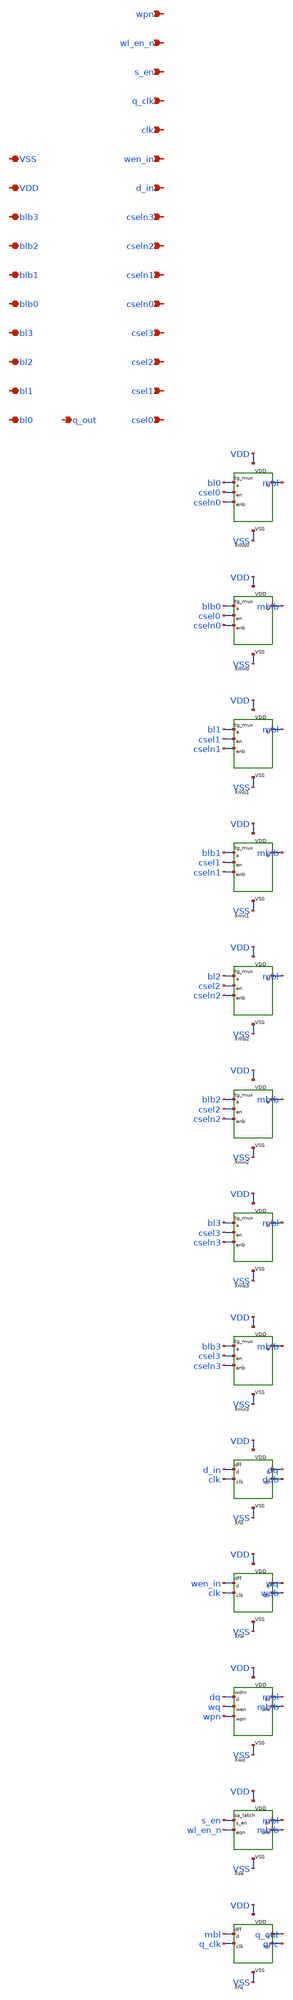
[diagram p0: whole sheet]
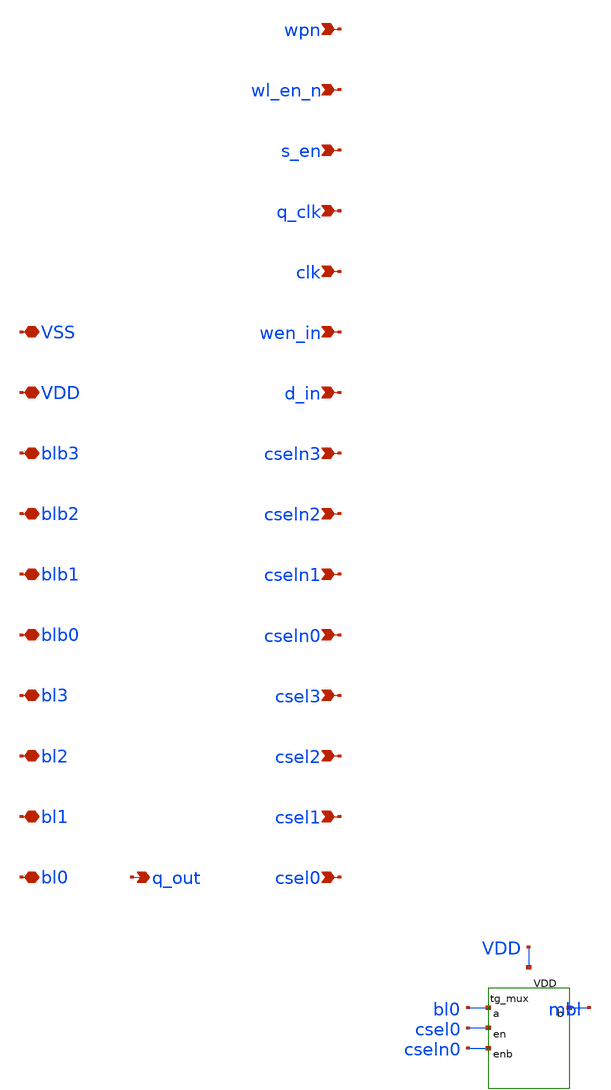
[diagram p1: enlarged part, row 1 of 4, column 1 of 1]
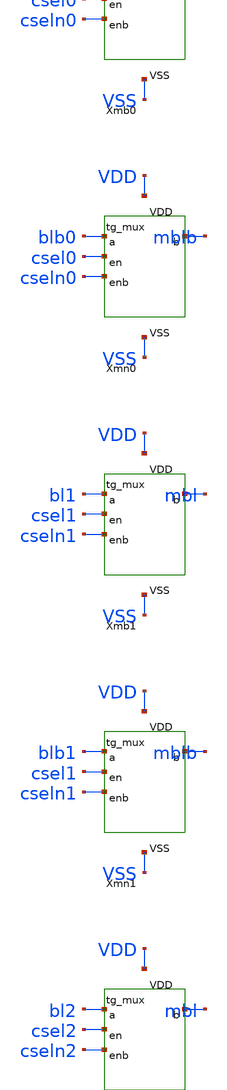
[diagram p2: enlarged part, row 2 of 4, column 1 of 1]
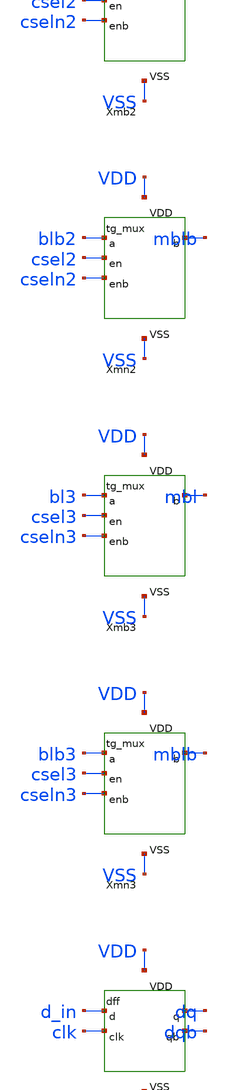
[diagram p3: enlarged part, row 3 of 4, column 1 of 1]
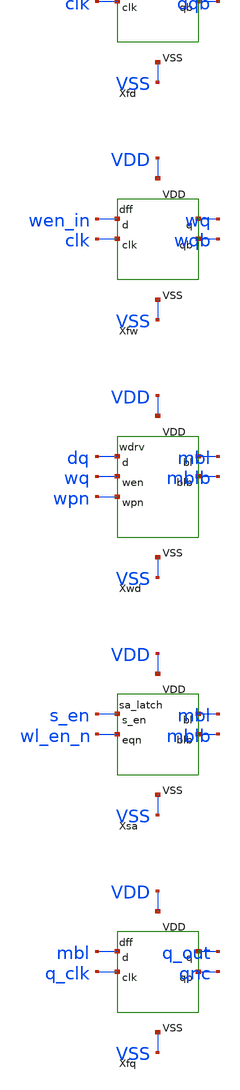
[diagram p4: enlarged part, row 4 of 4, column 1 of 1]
** sch_path: design/io_slice.sch
**.subckt io_slice csel0 csel1 csel2 csel3 cseln0 cseln1 cseln2 cseln3 d_in wen_in clk q_clk s_en
*+ wl_en_n wpn q_out bl0 bl1 bl2 bl3 blb0 blb1 blb2 blb3 VDD VSS
*.ipin csel0
*.ipin csel1
*.ipin csel2
*.ipin csel3
*.ipin cseln0
*.ipin cseln1
*.ipin cseln2
*.ipin cseln3
*.ipin d_in
*.ipin wen_in
*.ipin clk
*.ipin q_clk
*.ipin s_en
*.ipin wl_en_n
*.ipin wpn
*.opin q_out
*.iopin bl0
*.iopin bl1
*.iopin bl2
*.iopin bl3
*.iopin blb0
*.iopin blb1
*.iopin blb2
*.iopin blb3
*.iopin VDD
*.iopin VSS
XXmb0 bl0 csel0 cseln0 mbl VDD VSS tg_mux
XXmn0 blb0 csel0 cseln0 mblb VDD VSS tg_mux
XXmb1 bl1 csel1 cseln1 mbl VDD VSS tg_mux
XXmn1 blb1 csel1 cseln1 mblb VDD VSS tg_mux
XXmb2 bl2 csel2 cseln2 mbl VDD VSS tg_mux
XXmn2 blb2 csel2 cseln2 mblb VDD VSS tg_mux
XXmb3 bl3 csel3 cseln3 mbl VDD VSS tg_mux
XXmn3 blb3 csel3 cseln3 mblb VDD VSS tg_mux
XXfd d_in clk dq dqb VDD VSS dff
XXfw wen_in clk wq wqb VDD VSS dff
XXwd dq wq wpn mbl mblb VDD VSS wdrv
XXsa s_en wl_en_n mbl mblb VDD VSS sa_latch
XXfq mbl q_clk q_out qnc VDD VSS dff
**.ends

* expanding   symbol:  tg_mux.sym # of pins=6
** sym_path: design/tg_mux.sym
** sch_path: design/tg_mux.sch
.subckt tg_mux a en enb b VDD VSS

*.ipin a
*.ipin en
*.ipin enb
*.iopin b
*.iopin VDD
*.iopin VSS
XMN a en b VSS nfet_03v3 L=0.28u W=2u nf=1 ad='int((nf+1)/2) * W/nf * 0.18u' as='int((nf+2)/2) * W/nf * 0.18u'
+ pd='2*int((nf+1)/2) * (W/nf + 0.18u)' ps='2*int((nf+2)/2) * (W/nf + 0.18u)' nrd='0.18u / W' nrs='0.18u / W'
+ sa=0 sb=0 sd=0 m=1
XMP a enb b VDD pfet_03v3 L=0.28u W=3u nf=1 ad='int((nf+1)/2) * W/nf * 0.18u' as='int((nf+2)/2) * W/nf * 0.18u'
+ pd='2*int((nf+1)/2) * (W/nf + 0.18u)' ps='2*int((nf+2)/2) * (W/nf + 0.18u)' nrd='0.18u / W' nrs='0.18u / W'
+ sa=0 sb=0 sd=0 m=1
.ends


* expanding   symbol:  dff.sym # of pins=6
** sym_path: design/dff.sym
** sch_path: design/dff.sch
.subckt dff d clk q qb VDD VSS

*.ipin d
*.ipin clk
*.opin q
*.opin qb
*.iopin VDD
*.iopin VSS
XXckb clk ckb VDD VSS inv
XXckp ckb ckp VDD VSS inv
XXtm d ckb ckp m VDD VSS tg_s
XXnm m nm VDD VSS inv
XXmf nm mf VDD VSS inv
XXtmf mf ckp ckb m VDD VSS tg_s
XXts nm ckp ckb s VDD VSS tg_s
XXns s q VDD VSS inv
XXsf q qb VDD VSS inv
XXtsf qb ckb ckp s VDD VSS tg_s
.ends


* expanding   symbol:  wdrv.sym # of pins=7
** sym_path: design/wdrv.sym
** sch_path: design/wdrv.sch
.subckt wdrv d wen wpn bl blb VDD VSS

*.ipin d
*.ipin wen
*.ipin wpn
*.iopin bl
*.iopin blb
*.iopin VDD
*.iopin VSS
XMNWL bl pl VSS VSS nfet_03v3 L=0.28u W=1.5u nf=1 ad='int((nf+1)/2) * W/nf * 0.18u' as='int((nf+2)/2) * W/nf * 0.18u'
+ pd='2*int((nf+1)/2) * (W/nf + 0.18u)' ps='2*int((nf+2)/2) * (W/nf + 0.18u)' nrd='0.18u / W' nrs='0.18u / W'
+ sa=0 sb=0 sd=0 m=1
XMNWR blb pr VSS VSS nfet_03v3 L=0.28u W=1.5u nf=1 ad='int((nf+1)/2) * W/nf * 0.18u' as='int((nf+2)/2) * W/nf * 0.18u'
+ pd='2*int((nf+1)/2) * (W/nf + 0.18u)' ps='2*int((nf+2)/2) * (W/nf + 0.18u)' nrd='0.18u / W' nrs='0.18u / W'
+ sa=0 sb=0 sd=0 m=1
XXdn d dn VDD VSS inv
XXpl wen wpn d pl VDD VSS nor3
XXpr wen wpn dn pr VDD VSS nor3
.ends


* expanding   symbol:  sa_latch.sym # of pins=6
** sym_path: design/sa_latch.sym
** sch_path: design/sa_latch.sch
.subckt sa_latch s_en eqn bl blb VDD VSS

*.ipin s_en
*.ipin eqn
*.iopin bl
*.iopin blb
*.iopin VDD
*.iopin VSS
XMPA bl blb VDD VDD pfet_03v3 L=0.28u W=1u nf=1 ad='int((nf+1)/2) * W/nf * 0.18u' as='int((nf+2)/2) * W/nf * 0.18u'
+ pd='2*int((nf+1)/2) * (W/nf + 0.18u)' ps='2*int((nf+2)/2) * (W/nf + 0.18u)' nrd='0.18u / W' nrs='0.18u / W'
+ sa=0 sb=0 sd=0 m=1
XMPB blb bl VDD VDD pfet_03v3 L=0.28u W=1u nf=1 ad='int((nf+1)/2) * W/nf * 0.18u' as='int((nf+2)/2) * W/nf * 0.18u'
+ pd='2*int((nf+1)/2) * (W/nf + 0.18u)' ps='2*int((nf+2)/2) * (W/nf + 0.18u)' nrd='0.18u / W' nrs='0.18u / W'
+ sa=0 sb=0 sd=0 m=1
XMNA bl blb tail VSS nfet_03v3 L=0.28u W=1u nf=1 ad='int((nf+1)/2) * W/nf * 0.18u' as='int((nf+2)/2) * W/nf * 0.18u'
+ pd='2*int((nf+1)/2) * (W/nf + 0.18u)' ps='2*int((nf+2)/2) * (W/nf + 0.18u)' nrd='0.18u / W' nrs='0.18u / W'
+ sa=0 sb=0 sd=0 m=1
XMNB blb bl tail VSS nfet_03v3 L=0.28u W=1u nf=1 ad='int((nf+1)/2) * W/nf * 0.18u' as='int((nf+2)/2) * W/nf * 0.18u'
+ pd='2*int((nf+1)/2) * (W/nf + 0.18u)' ps='2*int((nf+2)/2) * (W/nf + 0.18u)' nrd='0.18u / W' nrs='0.18u / W'
+ sa=0 sb=0 sd=0 m=1
XMNT tail s_en VSS VSS nfet_03v3 L=0.28u W=2u nf=1 ad='int((nf+1)/2) * W/nf * 0.18u' as='int((nf+2)/2) * W/nf * 0.18u'
+ pd='2*int((nf+1)/2) * (W/nf + 0.18u)' ps='2*int((nf+2)/2) * (W/nf + 0.18u)' nrd='0.18u / W' nrs='0.18u / W'
+ sa=0 sb=0 sd=0 m=1
XMPE1 bl eqn VDD VDD pfet_03v3 L=0.28u W=1u nf=1 ad='int((nf+1)/2) * W/nf * 0.18u' as='int((nf+2)/2) * W/nf * 0.18u'
+ pd='2*int((nf+1)/2) * (W/nf + 0.18u)' ps='2*int((nf+2)/2) * (W/nf + 0.18u)' nrd='0.18u / W' nrs='0.18u / W'
+ sa=0 sb=0 sd=0 m=1
XMPE2 blb eqn VDD VDD pfet_03v3 L=0.28u W=1u nf=1 ad='int((nf+1)/2) * W/nf * 0.18u' as='int((nf+2)/2) * W/nf * 0.18u'
+ pd='2*int((nf+1)/2) * (W/nf + 0.18u)' ps='2*int((nf+2)/2) * (W/nf + 0.18u)' nrd='0.18u / W' nrs='0.18u / W'
+ sa=0 sb=0 sd=0 m=1
.ends


* expanding   symbol:  inv.sym # of pins=4
** sym_path: design/inv.sym
** sch_path: design/inv.sch
.subckt inv a y VDD VSS

*.ipin a
*.opin y
*.iopin VDD
*.iopin VSS
XMP y a VDD VDD pfet_03v3 L=0.28u W=1u nf=1 ad='int((nf+1)/2) * W/nf * 0.18u' as='int((nf+2)/2) * W/nf * 0.18u'
+ pd='2*int((nf+1)/2) * (W/nf + 0.18u)' ps='2*int((nf+2)/2) * (W/nf + 0.18u)' nrd='0.18u / W' nrs='0.18u / W'
+ sa=0 sb=0 sd=0 m=1
XMN y a VSS VSS nfet_03v3 L=0.28u W=0.5u nf=1 ad='int((nf+1)/2) * W/nf * 0.18u' as='int((nf+2)/2) * W/nf * 0.18u'
+ pd='2*int((nf+1)/2) * (W/nf + 0.18u)' ps='2*int((nf+2)/2) * (W/nf + 0.18u)' nrd='0.18u / W' nrs='0.18u / W'
+ sa=0 sb=0 sd=0 m=1
.ends


* expanding   symbol:  tg_s.sym # of pins=6
** sym_path: design/tg_s.sym
** sch_path: design/tg_s.sch
.subckt tg_s a en enb b VDD VSS

*.ipin a
*.ipin en
*.ipin enb
*.iopin b
*.iopin VDD
*.iopin VSS
XMN a en b VSS nfet_03v3 L=0.28u W=0.5u nf=1 ad='int((nf+1)/2) * W/nf * 0.18u' as='int((nf+2)/2) * W/nf * 0.18u'
+ pd='2*int((nf+1)/2) * (W/nf + 0.18u)' ps='2*int((nf+2)/2) * (W/nf + 0.18u)' nrd='0.18u / W' nrs='0.18u / W'
+ sa=0 sb=0 sd=0 m=1
XMP a enb b VDD pfet_03v3 L=0.28u W=1u nf=1 ad='int((nf+1)/2) * W/nf * 0.18u' as='int((nf+2)/2) * W/nf * 0.18u'
+ pd='2*int((nf+1)/2) * (W/nf + 0.18u)' ps='2*int((nf+2)/2) * (W/nf + 0.18u)' nrd='0.18u / W' nrs='0.18u / W'
+ sa=0 sb=0 sd=0 m=1
.ends


* expanding   symbol:  nor3.sym # of pins=6
** sym_path: design/nor3.sym
** sch_path: design/nor3.sch
.subckt nor3 a0 a1 a2 y VDD VSS

*.ipin a0
*.ipin a1
*.ipin a2
*.opin y
*.iopin VDD
*.iopin VSS
XMP0 t1 a0 VDD VDD pfet_03v3 L=0.28u W=2u nf=1 ad='int((nf+1)/2) * W/nf * 0.18u' as='int((nf+2)/2) * W/nf * 0.18u'
+ pd='2*int((nf+1)/2) * (W/nf + 0.18u)' ps='2*int((nf+2)/2) * (W/nf + 0.18u)' nrd='0.18u / W' nrs='0.18u / W'
+ sa=0 sb=0 sd=0 m=1
XMP1 t2 a1 t1 VDD pfet_03v3 L=0.28u W=2u nf=1 ad='int((nf+1)/2) * W/nf * 0.18u' as='int((nf+2)/2) * W/nf * 0.18u'
+ pd='2*int((nf+1)/2) * (W/nf + 0.18u)' ps='2*int((nf+2)/2) * (W/nf + 0.18u)' nrd='0.18u / W' nrs='0.18u / W'
+ sa=0 sb=0 sd=0 m=1
XMP2 y a2 t2 VDD pfet_03v3 L=0.28u W=2u nf=1 ad='int((nf+1)/2) * W/nf * 0.18u' as='int((nf+2)/2) * W/nf * 0.18u'
+ pd='2*int((nf+1)/2) * (W/nf + 0.18u)' ps='2*int((nf+2)/2) * (W/nf + 0.18u)' nrd='0.18u / W' nrs='0.18u / W'
+ sa=0 sb=0 sd=0 m=1
XMN0 y a0 VSS VSS nfet_03v3 L=0.28u W=0.5u nf=1 ad='int((nf+1)/2) * W/nf * 0.18u' as='int((nf+2)/2) * W/nf * 0.18u'
+ pd='2*int((nf+1)/2) * (W/nf + 0.18u)' ps='2*int((nf+2)/2) * (W/nf + 0.18u)' nrd='0.18u / W' nrs='0.18u / W'
+ sa=0 sb=0 sd=0 m=1
XMN1 y a1 VSS VSS nfet_03v3 L=0.28u W=0.5u nf=1 ad='int((nf+1)/2) * W/nf * 0.18u' as='int((nf+2)/2) * W/nf * 0.18u'
+ pd='2*int((nf+1)/2) * (W/nf + 0.18u)' ps='2*int((nf+2)/2) * (W/nf + 0.18u)' nrd='0.18u / W' nrs='0.18u / W'
+ sa=0 sb=0 sd=0 m=1
XMN2 y a2 VSS VSS nfet_03v3 L=0.28u W=0.5u nf=1 ad='int((nf+1)/2) * W/nf * 0.18u' as='int((nf+2)/2) * W/nf * 0.18u'
+ pd='2*int((nf+1)/2) * (W/nf + 0.18u)' ps='2*int((nf+2)/2) * (W/nf + 0.18u)' nrd='0.18u / W' nrs='0.18u / W'
+ sa=0 sb=0 sd=0 m=1
.ends

.end
